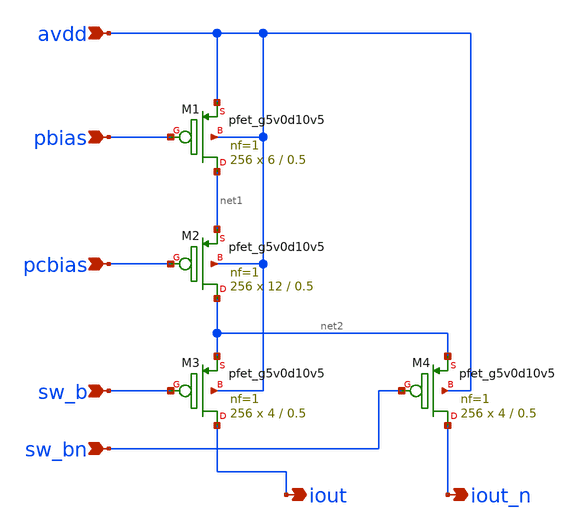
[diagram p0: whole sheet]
** sch_path: xschem/pcell256scs.sch
**.subckt pcell256scs pbias pcbias sw_b avdd iout iout_n sw_bn
*.ipin pbias
*.ipin pcbias
*.ipin sw_b
*.ipin avdd
*.opin iout
*.opin iout_n
*.ipin sw_bn
XM1 net1 pbias avdd avdd sky130_fd_pr__pfet_g5v0d10v5 L=0.5 W=6 nf=1 ad='int((nf+1)/2) * W/nf * 0.29'
+ as='int((nf+2)/2) * W/nf * 0.29' pd='2*int((nf+1)/2) * (W/nf + 0.29)' ps='2*int((nf+2)/2) * (W/nf + 0.29)'
+ nrd='0.29 / W' nrs='0.29 / W' sa=0 sb=0 sd=0 mult=256 m=256
XM2 net2 pcbias net1 avdd sky130_fd_pr__pfet_g5v0d10v5 L=0.5 W=12 nf=1 ad='int((nf+1)/2) * W/nf * 0.29'
+ as='int((nf+2)/2) * W/nf * 0.29' pd='2*int((nf+1)/2) * (W/nf + 0.29)' ps='2*int((nf+2)/2) * (W/nf + 0.29)'
+ nrd='0.29 / W' nrs='0.29 / W' sa=0 sb=0 sd=0 mult=256 m=256
XM3 iout sw_b net2 avdd sky130_fd_pr__pfet_g5v0d10v5 L=0.5 W=4 nf=1 ad='int((nf+1)/2) * W/nf * 0.29'
+ as='int((nf+2)/2) * W/nf * 0.29' pd='2*int((nf+1)/2) * (W/nf + 0.29)' ps='2*int((nf+2)/2) * (W/nf + 0.29)'
+ nrd='0.29 / W' nrs='0.29 / W' sa=0 sb=0 sd=0 mult=256 m=256
XM4 iout_n sw_bn net2 avdd sky130_fd_pr__pfet_g5v0d10v5 L=0.5 W=4 nf=1 ad='int((nf+1)/2) * W/nf * 0.29'
+ as='int((nf+2)/2) * W/nf * 0.29' pd='2*int((nf+1)/2) * (W/nf + 0.29)' ps='2*int((nf+2)/2) * (W/nf + 0.29)'
+ nrd='0.29 / W' nrs='0.29 / W' sa=0 sb=0 sd=0 mult=256 m=256
**.ends
.end
